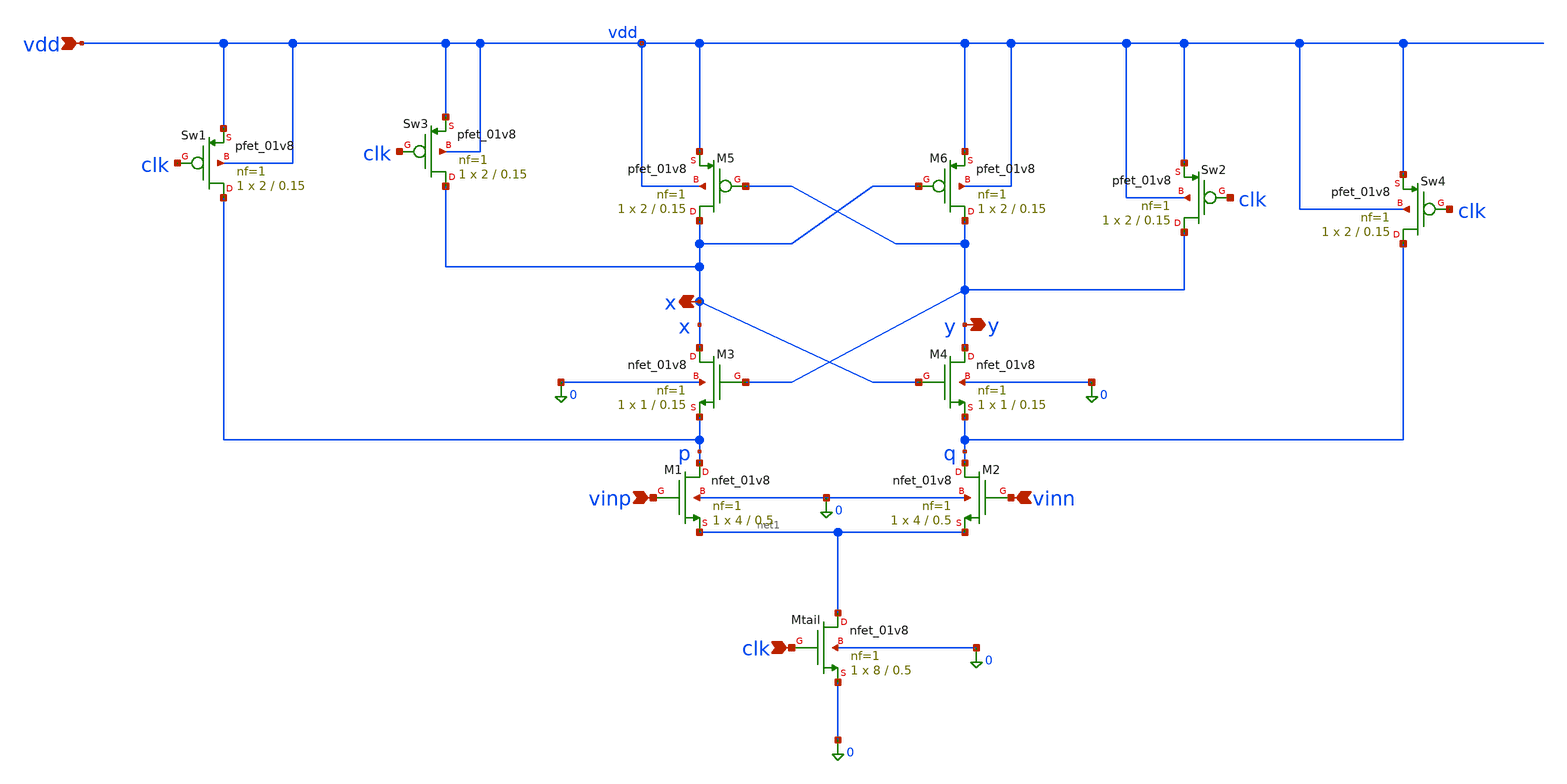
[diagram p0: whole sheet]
** sch_path: sch/comparator.sch
**.subckt comparator vinp vinn y x vdd clk
*.ipin vinp
*.ipin vinn
*.opin y
*.opin x
*.ipin vdd
*.ipin clk
XM1 p vinp net1 0 sky130_fd_pr__nfet_01v8 L=0.5 W=4 nf=1 ad='int((1 + 1)/2) * 4 / 1 * 0.29' as='int((1 + 2)/2) * 4 / 1 * 0.29'
+ pd='2*int((1 + 1)/2) * (4 / 1 + 0.29)' ps='2*int((1 + 2)/2) * (4 / 1 + 0.29)' nrd='0.29 / 4 ' nrs='0.29 / 4 '
+ sa=0 sb=0 sd=0 mult=1 m=1
XM2 q vinn net1 0 sky130_fd_pr__nfet_01v8 L=0.5 W=4 nf=1 ad='int((1 + 1)/2) * 4 / 1 * 0.29' as='int((1 + 2)/2) * 4 / 1 * 0.29'
+ pd='2*int((1 + 1)/2) * (4 / 1 + 0.29)' ps='2*int((1 + 2)/2) * (4 / 1 + 0.29)' nrd='0.29 / 4 ' nrs='0.29 / 4 '
+ sa=0 sb=0 sd=0 mult=1 m=1
XMtail net1 clk 0 0 sky130_fd_pr__nfet_01v8 L=0.5 W=8 nf=1 ad='int((1 + 1)/2) * 8 / 1 * 0.29' as='int((1 + 2)/2) * 8 / 1 * 0.29'
+ pd='2*int((1 + 1)/2) * (8 / 1 + 0.29)' ps='2*int((1 + 2)/2) * (8 / 1 + 0.29)' nrd='0.29 / 8 ' nrs='0.29 / 8 '
+ sa=0 sb=0 sd=0 mult=1 m=1
XM4 y x q 0 sky130_fd_pr__nfet_01v8 L=0.15 W=1 nf=1 ad='int((1 + 1)/2) * 1 / 1 * 0.29' as='int((1 + 2)/2) * 1 / 1 * 0.29'
+ pd='2*int((1 + 1)/2) * (1 / 1 + 0.29)' ps='2*int((1 + 2)/2) * (1 / 1 + 0.29)' nrd='0.29 / 1 ' nrs='0.29 / 1 '
+ sa=0 sb=0 sd=0 mult=1 m=1
XM3 x y p 0 sky130_fd_pr__nfet_01v8 L=0.15 W=1 nf=1 ad='int((1 + 1)/2) * 1 / 1 * 0.29' as='int((1 + 2)/2) * 1 / 1 * 0.29'
+ pd='2*int((1 + 1)/2) * (1 / 1 + 0.29)' ps='2*int((1 + 2)/2) * (1 / 1 + 0.29)' nrd='0.29 / 1 ' nrs='0.29 / 1 '
+ sa=0 sb=0 sd=0 mult=1 m=1
XM5 x y vdd vdd sky130_fd_pr__pfet_01v8 L=0.15 W=2 nf=1 ad='int((1 + 1)/2) * 2 / 1 * 0.29' as='int((1 + 2)/2) * 2 / 1 * 0.29'
+ pd='2*int((1 + 1)/2) * (2 / 1 + 0.29)' ps='2*int((1 + 2)/2) * (2 / 1 + 0.29)' nrd='0.29 / 2 ' nrs='0.29 / 2 '
+ sa=0 sb=0 sd=0 mult=1 m=1
XM6 y x vdd vdd sky130_fd_pr__pfet_01v8 L=0.15 W=2 nf=1 ad='int((1 + 1)/2) * 2 / 1 * 0.29' as='int((1 + 2)/2) * 2 / 1 * 0.29'
+ pd='2*int((1 + 1)/2) * (2 / 1 + 0.29)' ps='2*int((1 + 2)/2) * (2 / 1 + 0.29)' nrd='0.29 / 2 ' nrs='0.29 / 2 '
+ sa=0 sb=0 sd=0 mult=1 m=1
XSw1 p clk vdd vdd sky130_fd_pr__pfet_01v8 L=0.15 W=2 nf=1 ad='int((1 + 1)/2) * 2 / 1 * 0.29' as='int((1 + 2)/2) * 2 / 1 * 0.29'
+ pd='2*int((1 + 1)/2) * (2 / 1 + 0.29)' ps='2*int((1 + 2)/2) * (2 / 1 + 0.29)' nrd='0.29 / 2 ' nrs='0.29 / 2 '
+ sa=0 sb=0 sd=0 mult=1 m=1
XSw3 x clk vdd vdd sky130_fd_pr__pfet_01v8 L=0.15 W=2 nf=1 ad='int((1 + 1)/2) * 2 / 1 * 0.29' as='int((1 + 2)/2) * 2 / 1 * 0.29'
+ pd='2*int((1 + 1)/2) * (2 / 1 + 0.29)' ps='2*int((1 + 2)/2) * (2 / 1 + 0.29)' nrd='0.29 / 2 ' nrs='0.29 / 2 '
+ sa=0 sb=0 sd=0 mult=1 m=1
XSw2 y clk vdd vdd sky130_fd_pr__pfet_01v8 L=0.15 W=2 nf=1 ad='int((1 + 1)/2) * 2 / 1 * 0.29' as='int((1 + 2)/2) * 2 / 1 * 0.29'
+ pd='2*int((1 + 1)/2) * (2 / 1 + 0.29)' ps='2*int((1 + 2)/2) * (2 / 1 + 0.29)' nrd='0.29 / 2 ' nrs='0.29 / 2 '
+ sa=0 sb=0 sd=0 mult=1 m=1
XSw4 q clk vdd vdd sky130_fd_pr__pfet_01v8 L=0.15 W=2 nf=1 ad='int((1 + 1)/2) * 2 / 1 * 0.29' as='int((1 + 2)/2) * 2 / 1 * 0.29'
+ pd='2*int((1 + 1)/2) * (2 / 1 + 0.29)' ps='2*int((1 + 2)/2) * (2 / 1 + 0.29)' nrd='0.29 / 2 ' nrs='0.29 / 2 '
+ sa=0 sb=0 sd=0 mult=1 m=1
**.ends
.end
